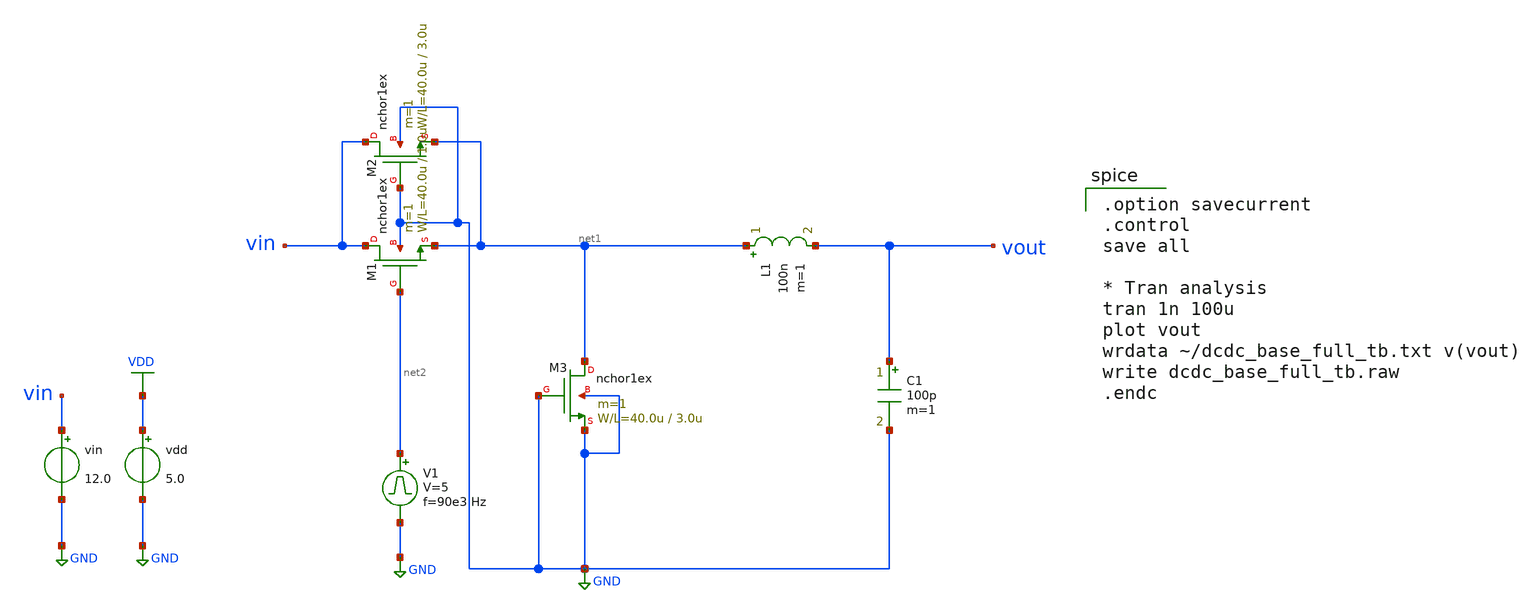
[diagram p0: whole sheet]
** sch_path: member_project/DCDC_DOWN/xschem/dcdc_base_full_tb.sch
**.subckt dcdc_base_full_tb
vin vin GND 12.0
M1 vin net2 net1 GND nchor1ex L=1.0u W=40.0u m=1
L1 net1 vout 100n m=1
V1 net2 GND pulse 0 5 '0.495/ 90e3 ' '0.01/90e3 ' '0.01/90e3 ' '0.49/90e3 ' '1/90e3 '
vdd VDD GND 5.0
C1 vout GND 100p m=1
M2 vin GND net1 GND nchor1ex L=3.0u W=40.0u m=1
M3 net1 GND GND GND nchor1ex L=3.0u W=40.0u m=1
**** begin user architecture code
 .include $::LIB/mos.lib
.include $::LIB/passive.lib
.include $::LIB/diode.lib

.option savecurrent
.control
save all

* Tran analysis
tran 1n 100u
plot vout
wrdata ~/dcdc_base_full_tb.txt v(vout)
write dcdc_base_full_tb.raw
.endc

**** end user architecture code
**.ends
.GLOBAL GND
.GLOBAL VDD
.end
